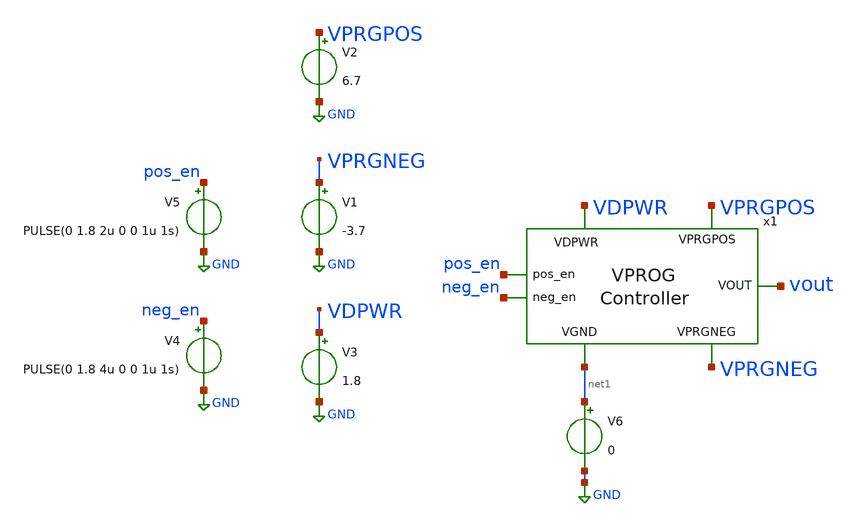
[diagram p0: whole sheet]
** sch_path: xschem/vprog_controller_tb.sch
**.subckt vprog_controller_tb
V1 VPRGNEG GND -3.7
V3 VDPWR GND 1.8
x1 VDPWR vout VPRGNEG net1 VPRGPOS pos_en neg_en vprog_controller
V4 neg_en GND PULSE(0 1.8 4u 0 0 1u 1s)
V5 pos_en GND PULSE(0 1.8 2u 0 0 1u 1s)
V2 VPRGPOS GND 6.7
V6 net1 GND 0
**** begin user architecture code

** opencircuitdesign pdks install
.lib $::SKYWATER_MODELS/sky130.lib.spice tt
.include ../../spice/vprog_controller/pex/vprog_controller.spice
*.include ../../spice/vprog_controller/sch/vprog_controller.spice




.option savecurrents
.tran 1n 10u
.save all

.control
run
remzerovec
write vprog_controller_tb.raw
.endc


**** end user architecture code
**.ends

* expanding   symbol:  vprog_controller.sym # of pins=7
** sym_path: xschem/vprog_controller.sym
** sch_path: xschem/vprog_controller.sch
.subckt vprog_controller VDPWR VOUT VPRGNEG VGND VPRGPOS pos_en neg_en
*.iopin VPRGNEG
*.ipin neg_en
*.opin VOUT
*.iopin VDPWR
*.ipin pos_en
*.iopin VGND
*.iopin VPRGPOS
XM6 neg_en_b neg_en VGND VGND sky130_fd_pr__nfet_01v8 L=3 W=1 nf=1 ad='int((nf+1)/2) * W/nf * 0.29' as='int((nf+2)/2) * W/nf * 0.29'
+ pd='2*int((nf+1)/2) * (W/nf + 0.29)' ps='2*int((nf+2)/2) * (W/nf + 0.29)' nrd='0.29 / W' nrs='0.29 / W'
+ sa=0 sb=0 sd=0 mult=1 m=1
XM5 neg_en_b neg_en VDPWR VDPWR sky130_fd_pr__pfet_01v8 L=3 W=1 nf=1 ad='int((nf+1)/2) * W/nf * 0.29'
+ as='int((nf+2)/2) * W/nf * 0.29' pd='2*int((nf+1)/2) * (W/nf + 0.29)' ps='2*int((nf+2)/2) * (W/nf + 0.29)'
+ nrd='0.29 / W' nrs='0.29 / W' sa=0 sb=0 sd=0 mult=1 m=1
XM1 net1 neg_en VDPWR VDPWR sky130_fd_pr__pfet_g5v0d10v5 L=0.5 W=3 nf=1 ad='int((nf+1)/2) * W/nf * 0.29'
+ as='int((nf+2)/2) * W/nf * 0.29' pd='2*int((nf+1)/2) * (W/nf + 0.29)' ps='2*int((nf+2)/2) * (W/nf + 0.29)'
+ nrd='0.29 / W' nrs='0.29 / W' sa=0 sb=0 sd=0 mult=1 m=1
XM2 neg_mid_b neg_en_b VDPWR VDPWR sky130_fd_pr__pfet_g5v0d10v5 L=0.5 W=3 nf=1 ad='int((nf+1)/2) * W/nf * 0.29'
+ as='int((nf+2)/2) * W/nf * 0.29' pd='2*int((nf+1)/2) * (W/nf + 0.29)' ps='2*int((nf+2)/2) * (W/nf + 0.29)'
+ nrd='0.29 / W' nrs='0.29 / W' sa=0 sb=0 sd=0 mult=1 m=1
XM4 neg_mid_b net1 VPRGNEG VPRGNEG sky130_fd_pr__nfet_g5v0d10v5 L=2 W=0.5 nf=1 ad='int((nf+1)/2) * W/nf * 0.29'
+ as='int((nf+2)/2) * W/nf * 0.29' pd='2*int((nf+1)/2) * (W/nf + 0.29)' ps='2*int((nf+2)/2) * (W/nf + 0.29)'
+ nrd='0.29 / W' nrs='0.29 / W' sa=0 sb=0 sd=0 mult=1 m=1
XM3 net1 neg_mid_b VPRGNEG VPRGNEG sky130_fd_pr__nfet_g5v0d10v5 L=2 W=0.5 nf=1 ad='int((nf+1)/2) * W/nf * 0.29'
+ as='int((nf+2)/2) * W/nf * 0.29' pd='2*int((nf+1)/2) * (W/nf + 0.29)' ps='2*int((nf+2)/2) * (W/nf + 0.29)'
+ nrd='0.29 / W' nrs='0.29 / W' sa=0 sb=0 sd=0 mult=1 m=1
XM7 VOUT neg_mid_b VPRGNEG VPRGNEG sky130_fd_pr__nfet_g5v0d10v5 L=3 W=1 nf=1 ad='int((nf+1)/2) * W/nf * 0.29'
+ as='int((nf+2)/2) * W/nf * 0.29' pd='2*int((nf+1)/2) * (W/nf + 0.29)' ps='2*int((nf+2)/2) * (W/nf + 0.29)'
+ nrd='0.29 / W' nrs='0.29 / W' sa=0 sb=0 sd=0 mult=1 m=1
XM9 pos_en_b pos_en VGND VGND sky130_fd_pr__nfet_01v8 L=3 W=1 nf=1 ad='int((nf+1)/2) * W/nf * 0.29' as='int((nf+2)/2) * W/nf * 0.29'
+ pd='2*int((nf+1)/2) * (W/nf + 0.29)' ps='2*int((nf+2)/2) * (W/nf + 0.29)' nrd='0.29 / W' nrs='0.29 / W'
+ sa=0 sb=0 sd=0 mult=1 m=1
XM10 pos_en_b pos_en VDPWR VDPWR sky130_fd_pr__pfet_01v8 L=3 W=1 nf=1 ad='int((nf+1)/2) * W/nf * 0.29'
+ as='int((nf+2)/2) * W/nf * 0.29' pd='2*int((nf+1)/2) * (W/nf + 0.29)' ps='2*int((nf+2)/2) * (W/nf + 0.29)'
+ nrd='0.29 / W' nrs='0.29 / W' sa=0 sb=0 sd=0 mult=1 m=1
XM8 net2 pos_en_b VGND VGND sky130_fd_pr__nfet_g5v0d10v5 L=1 W=0.5 nf=1 ad='int((nf+1)/2) * W/nf * 0.29'
+ as='int((nf+2)/2) * W/nf * 0.29' pd='2*int((nf+1)/2) * (W/nf + 0.29)' ps='2*int((nf+2)/2) * (W/nf + 0.29)'
+ nrd='0.29 / W' nrs='0.29 / W' sa=0 sb=0 sd=0 mult=1 m=1
XM12 net3 pos_mid_b VPRGPOS VPRGPOS sky130_fd_pr__pfet_g5v0d10v5 L=3 W=1 nf=1 ad='int((nf+1)/2) * W/nf * 0.29'
+ as='int((nf+2)/2) * W/nf * 0.29' pd='2*int((nf+1)/2) * (W/nf + 0.29)' ps='2*int((nf+2)/2) * (W/nf + 0.29)'
+ nrd='0.29 / W' nrs='0.29 / W' sa=0 sb=0 sd=0 mult=1 m=1
XM13 pos_mid_b net3 VPRGPOS VPRGPOS sky130_fd_pr__pfet_g5v0d10v5 L=3 W=1 nf=1 ad='int((nf+1)/2) * W/nf * 0.29'
+ as='int((nf+2)/2) * W/nf * 0.29' pd='2*int((nf+1)/2) * (W/nf + 0.29)' ps='2*int((nf+2)/2) * (W/nf + 0.29)'
+ nrd='0.29 / W' nrs='0.29 / W' sa=0 sb=0 sd=0 mult=1 m=1
XM14 pos_mid_b pos_en VGND VGND sky130_fd_pr__nfet_g5v0d10v5 L=3 W=2 nf=1 ad='int((nf+1)/2) * W/nf * 0.29'
+ as='int((nf+2)/2) * W/nf * 0.29' pd='2*int((nf+1)/2) * (W/nf + 0.29)' ps='2*int((nf+2)/2) * (W/nf + 0.29)'
+ nrd='0.29 / W' nrs='0.29 / W' sa=0 sb=0 sd=0 mult=1 m=1
XM15 net3 pos_en_b VGND VGND sky130_fd_pr__nfet_g5v0d10v5 L=3 W=2 nf=1 ad='int((nf+1)/2) * W/nf * 0.29'
+ as='int((nf+2)/2) * W/nf * 0.29' pd='2*int((nf+1)/2) * (W/nf + 0.29)' ps='2*int((nf+2)/2) * (W/nf + 0.29)'
+ nrd='0.29 / W' nrs='0.29 / W' sa=0 sb=0 sd=0 mult=1 m=1
XM16 VOUT pos_mid_b VPRGPOS VPRGPOS sky130_fd_pr__pfet_g5v0d10v5 L=0.5 W=3 nf=1 ad='int((nf+1)/2) * W/nf * 0.29'
+ as='int((nf+2)/2) * W/nf * 0.29' pd='2*int((nf+1)/2) * (W/nf + 0.29)' ps='2*int((nf+2)/2) * (W/nf + 0.29)'
+ nrd='0.29 / W' nrs='0.29 / W' sa=0 sb=0 sd=0 mult=1 m=1
XM11 VOUT neg_mid_b net2 net2 sky130_fd_pr__pfet_g5v0d10v5 L=0.5 W=3 nf=1 ad='int((nf+1)/2) * W/nf * 0.29'
+ as='int((nf+2)/2) * W/nf * 0.29' pd='2*int((nf+1)/2) * (W/nf + 0.29)' ps='2*int((nf+2)/2) * (W/nf + 0.29)'
+ nrd='0.29 / W' nrs='0.29 / W' sa=0 sb=0 sd=0 mult=1 m=1
.ends

.GLOBAL GND
.end
